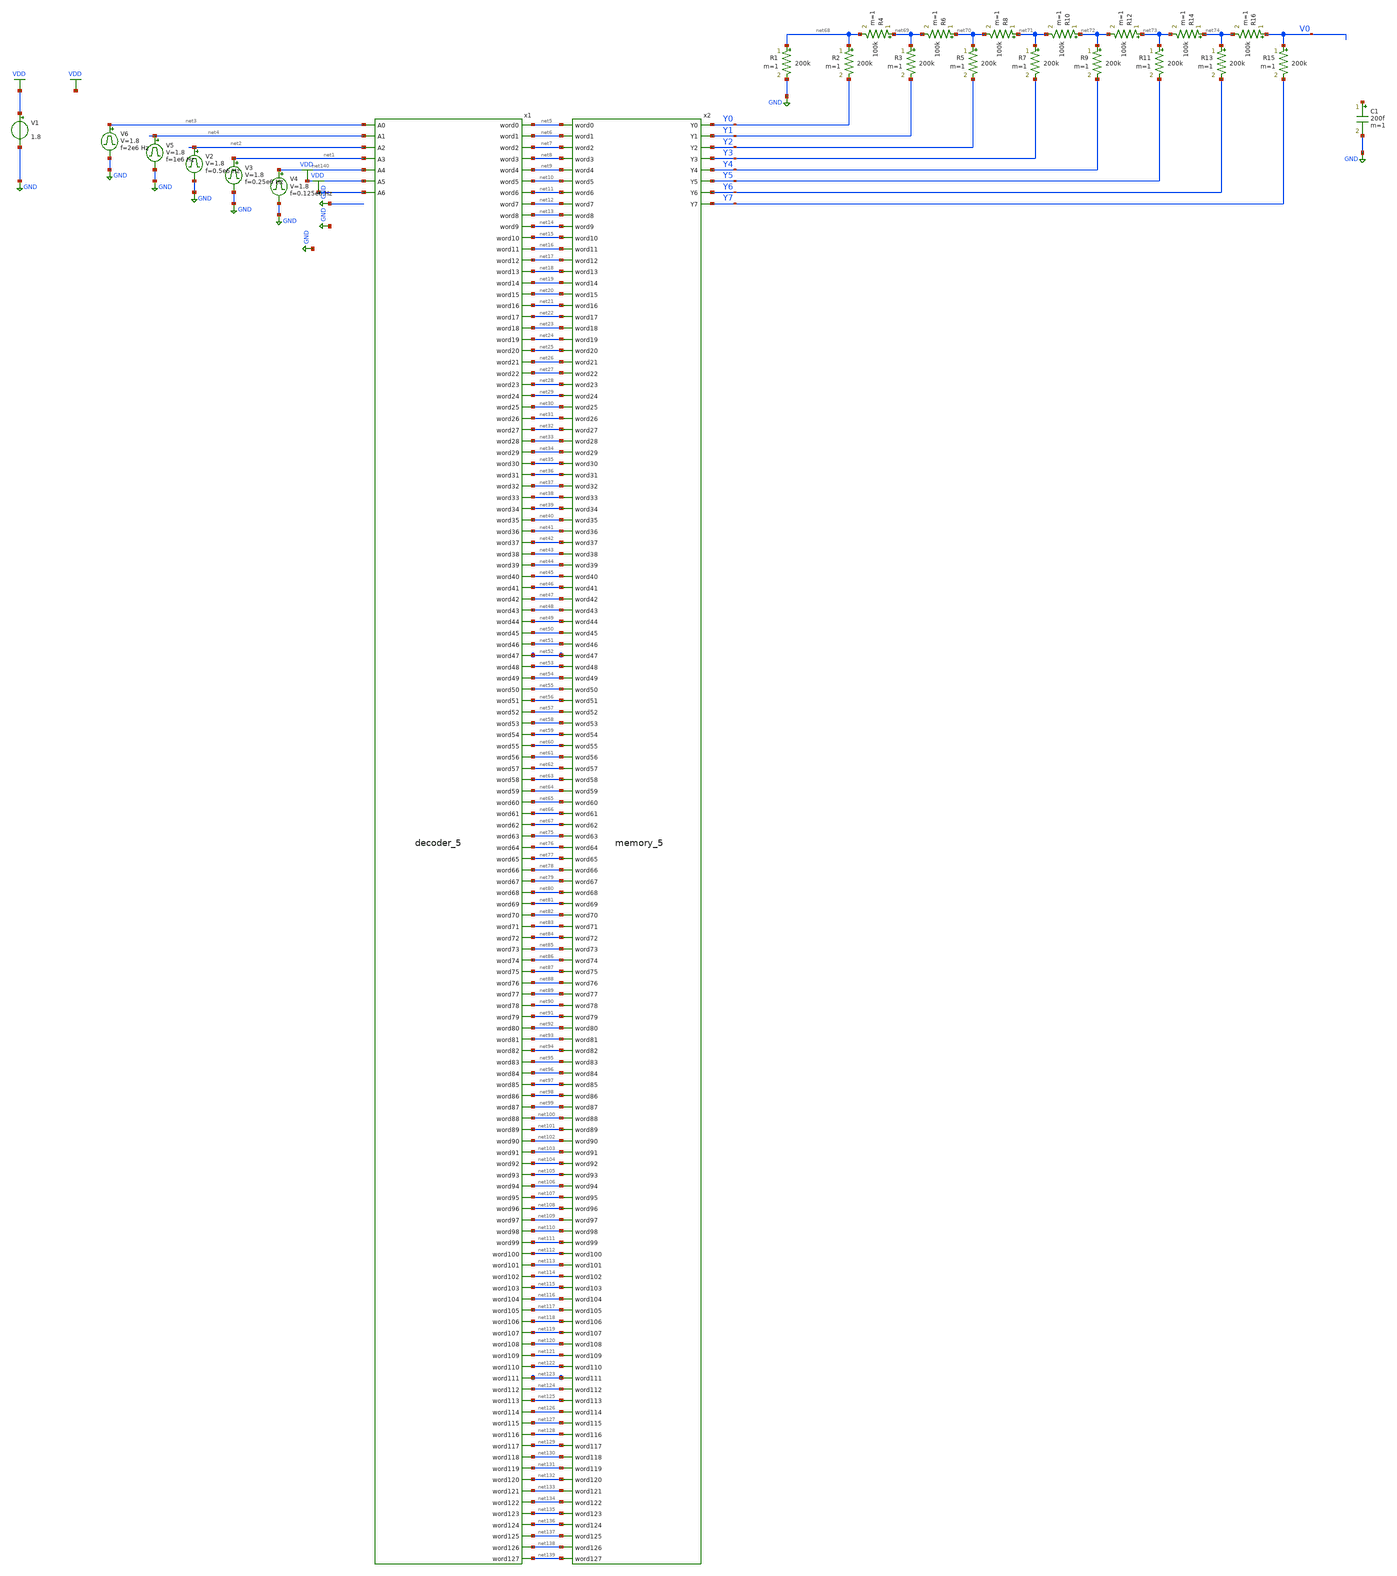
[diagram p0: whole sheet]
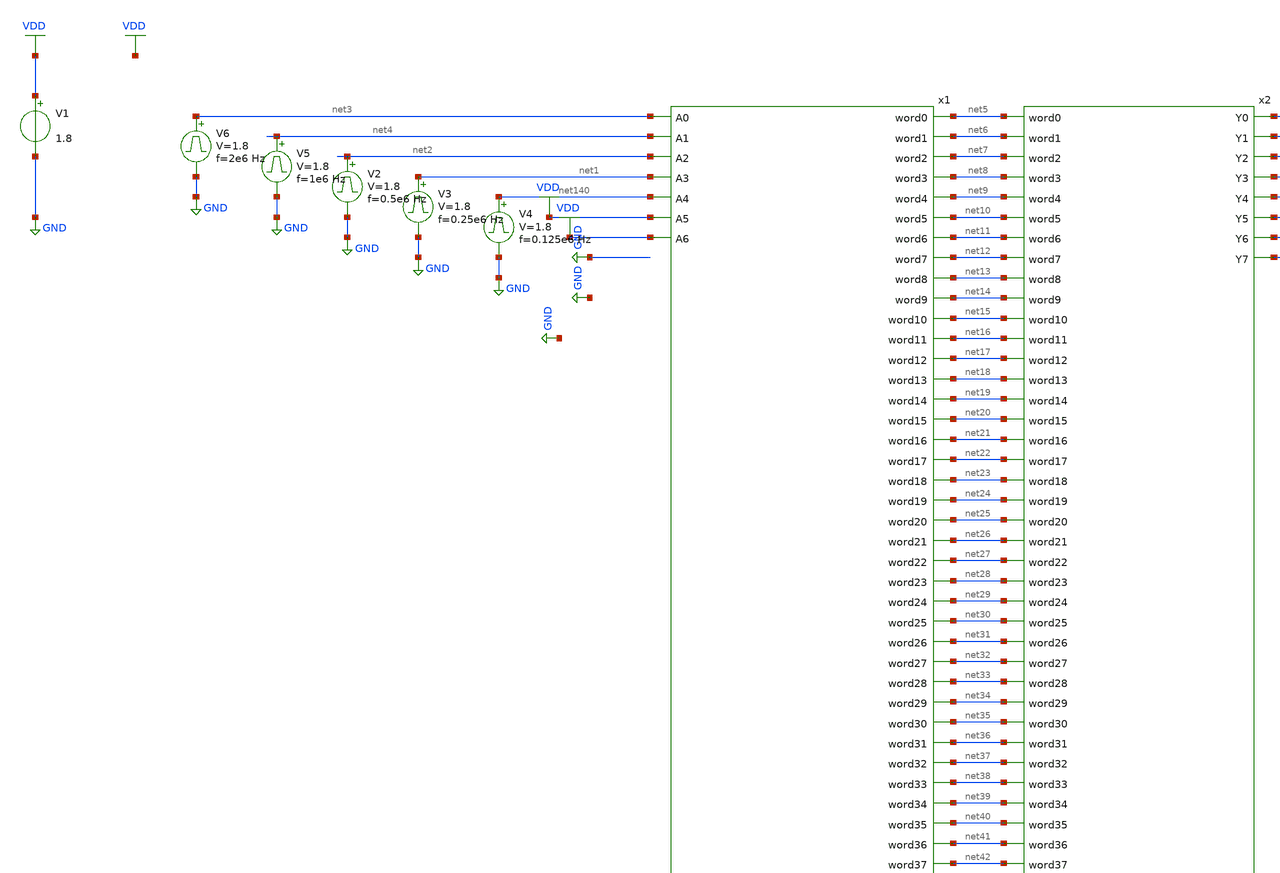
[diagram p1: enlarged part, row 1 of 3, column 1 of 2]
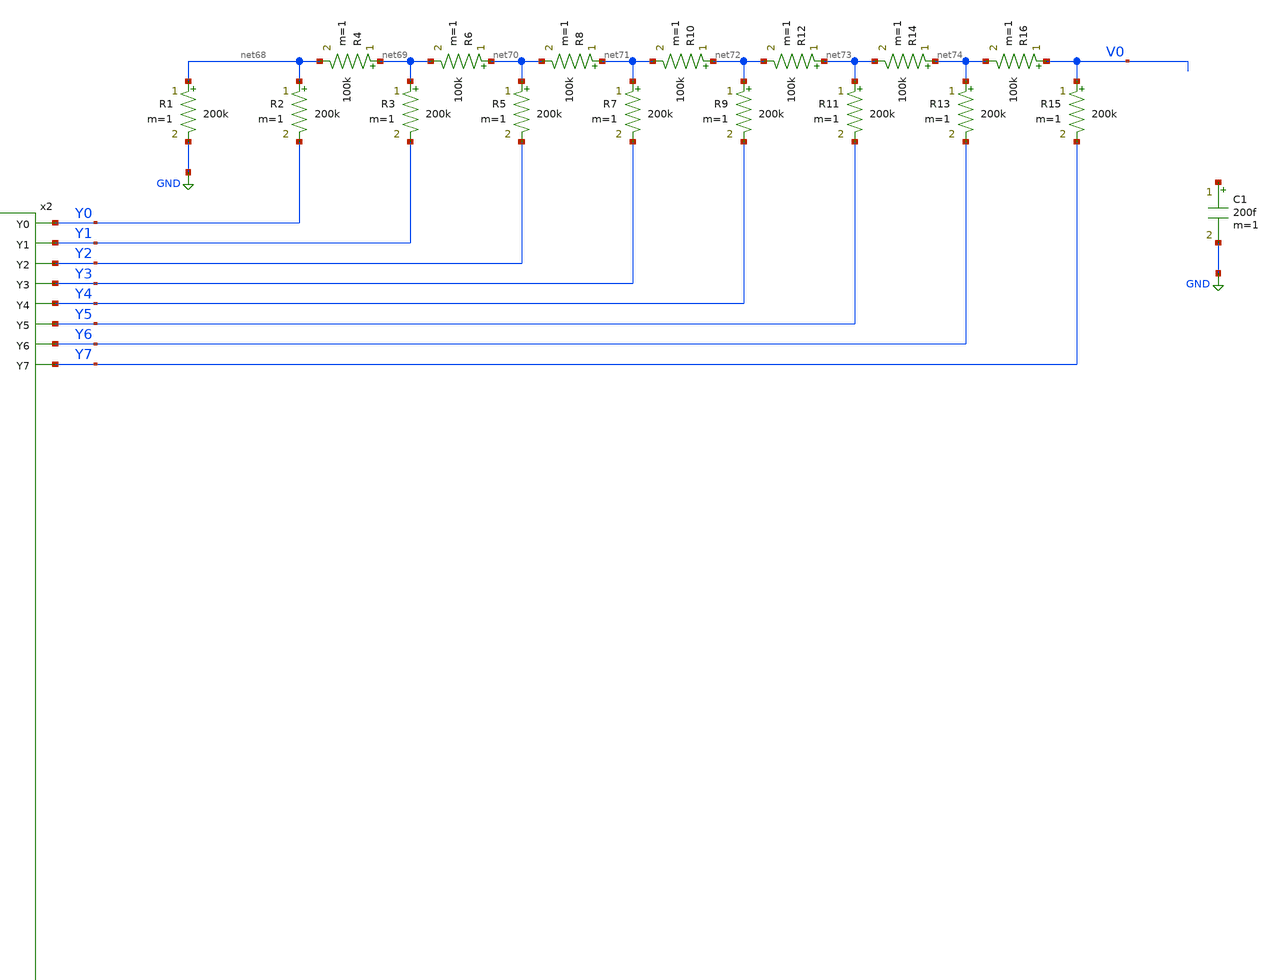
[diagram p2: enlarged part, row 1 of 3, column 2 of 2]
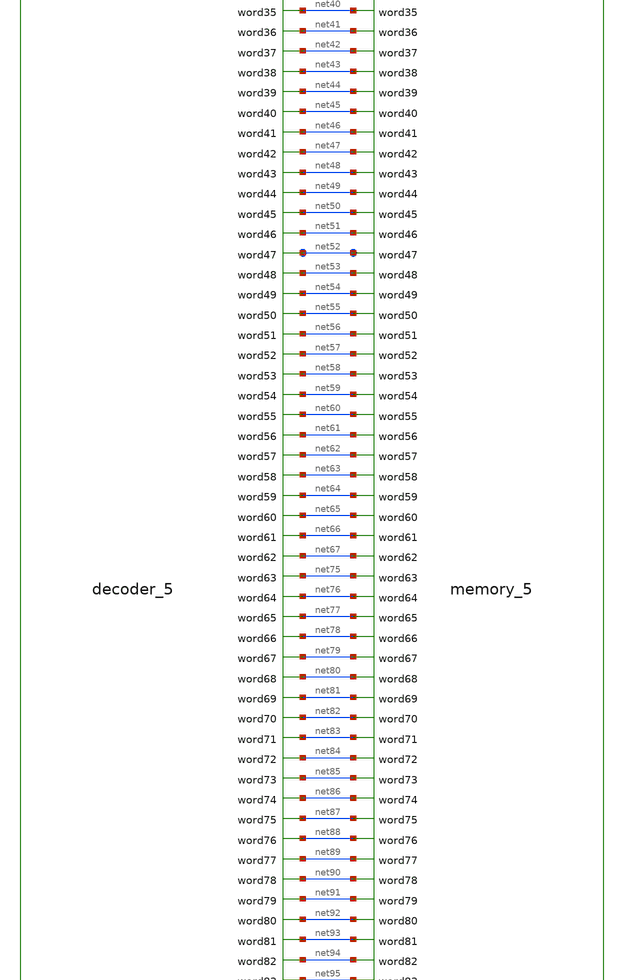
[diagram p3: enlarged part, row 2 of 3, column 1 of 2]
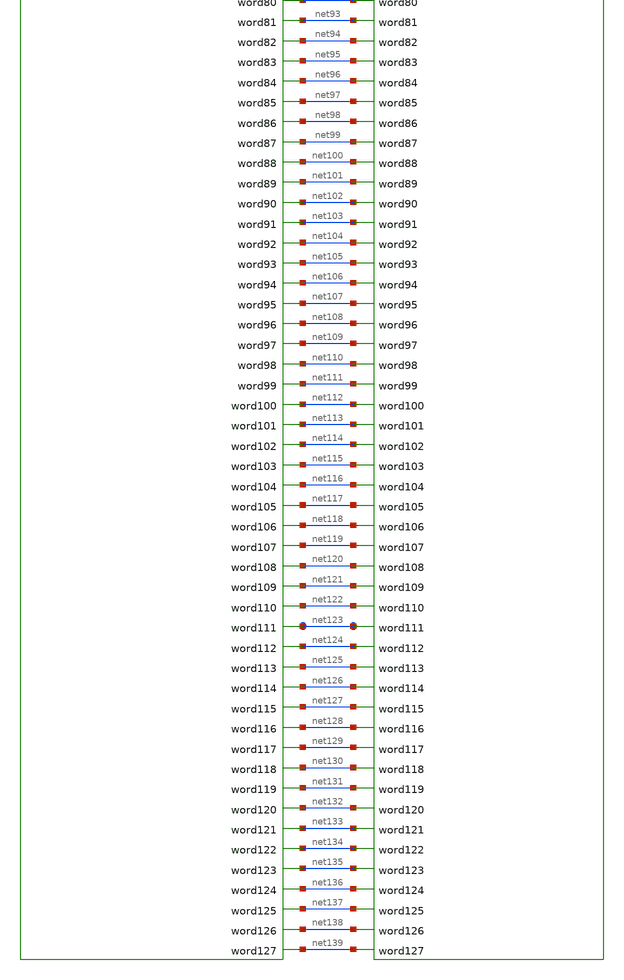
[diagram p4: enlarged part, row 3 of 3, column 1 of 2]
** sch_path: circuits/xschem/testing/decoder_memory_5_tb.sch
**.subckt decoder_memory_5_tb
V1 VDD GND 1.8
V2 net2 GND pulse 0 1.8 '0.495/ 0.5e6 ' '0.01/0.5e6 ' '0.01/0.5e6 ' '0.49/0.5e6 ' '1/0.5e6 '
V3 net1 GND pulse 0 1.8 '0.495/ 0.25e6 ' '0.01/0.25e6 ' '0.01/0.25e6 ' '0.49/0.25e6 ' '1/0.25e6 '
V4 net140 GND pulse 0 1.8 '0.495/ 0.125e6 ' '0.01/0.125e6 ' '0.01/0.125e6 ' '0.49/0.125e6 ' '1/0.125e6 '
V5 net4 GND pulse 0 1.8 '0.495/ 1e6 ' '0.01/1e6 ' '0.01/1e6 ' '0.49/1e6 ' '1/1e6 '
R1 net68 GND 200k m=1
R2 net68 Y0 200k m=1
R3 net69 Y1 200k m=1
R4 net69 net68 100k m=1
R5 net70 Y2 200k m=1
R6 net70 net69 100k m=1
R7 net71 Y3 200k m=1
R8 net71 net70 100k m=1
R9 net72 Y4 200k m=1
R10 net72 net71 100k m=1
R11 net73 Y5 200k m=1
R12 net73 net72 100k m=1
R13 net74 Y6 200k m=1
R14 net74 net73 100k m=1
R15 V0 Y7 200k m=1
R16 V0 net74 100k m=1
C1 net141 GND 200f m=1
x1 net4 VDD net1 net140 net2 VDD net3 net5 net6 net7 net8 net9 net10 net11 net12 net13 net14 net15
+ net16 net17 net18 net19 net20 net21 net22 net23 net24 net25 net26 net27 net28 net29 net30 net31 net32
+ net33 net34 net35 net36 net37 net38 net39 net40 net41 net42 net43 net44 net45 net46 net47 net48 net49
+ net50 net51 net52 net53 net54 net55 net56 net57 net58 net59 net60 net61 net62 net63 net64 net65 net66
+ net67 net75 net76 net77 net78 net79 net80 net81 net82 net83 net84 net85 net86 net87 net88 net89 net90
+ net91 net92 net93 net94 net95 net96 net97 net98 net99 net100 net101 net102 net103 net104 net105 net106
+ net107 net108 net109 net110 net111 net112 net113 net114 net115 net116 net117 net118 net119 net120 net121
+ net122 net123 net124 net125 net126 net127 net128 net129 net130 net131 net132 net133 net134 net135 net136
+ net137 net138 net139 decoder_5
x2 net5 net6 net7 net8 net9 net10 net11 net12 net13 net14 net15 net16 net17 net18 net19 net20 net21
+ net22 net23 net24 net25 net26 net27 net28 net29 net30 net31 net32 net33 net34 net35 net36 net37 net38
+ net39 net40 net41 net42 net43 net44 net45 net46 net47 net48 net49 net50 net51 net52 net53 net54 net55
+ net56 net57 net58 net59 net60 net61 net62 net63 net64 net65 net66 net67 net75 net76 net77 net78 net79
+ net80 net81 net82 net83 net84 net85 net86 net87 net88 net89 net90 net91 net92 net93 net94 net95 net96
+ net97 net98 net99 net100 net101 net102 net103 net104 net105 net106 net107 net108 net109 net110 net111
+ net112 net113 net114 net115 net116 net117 net118 net119 net120 net121 net122 net123 net124 net125 net126
+ net127 net128 net129 net130 net131 net132 net133 net134 net135 net136 net137 net138 net139 Y0 Y1 Y2 Y3 Y4
+ Y5 Y6 Y7 memory_5
V6 net3 GND pulse 0 1.8 '0.495/ 2e6 ' '0.01/2e6 ' '0.01/2e6 ' '0.49/2e6 ' '1/2e6 '
**** begin user architecture code


.control
save all
tran 1n 8u uic
plot V(V0)
.endc



** opencircuitdesign pdks install
.lib $::SKYWATER_MODELS/sky130.lib.spice tt


**** end user architecture code
**.ends
.GLOBAL VDD
.GLOBAL GND
.end
